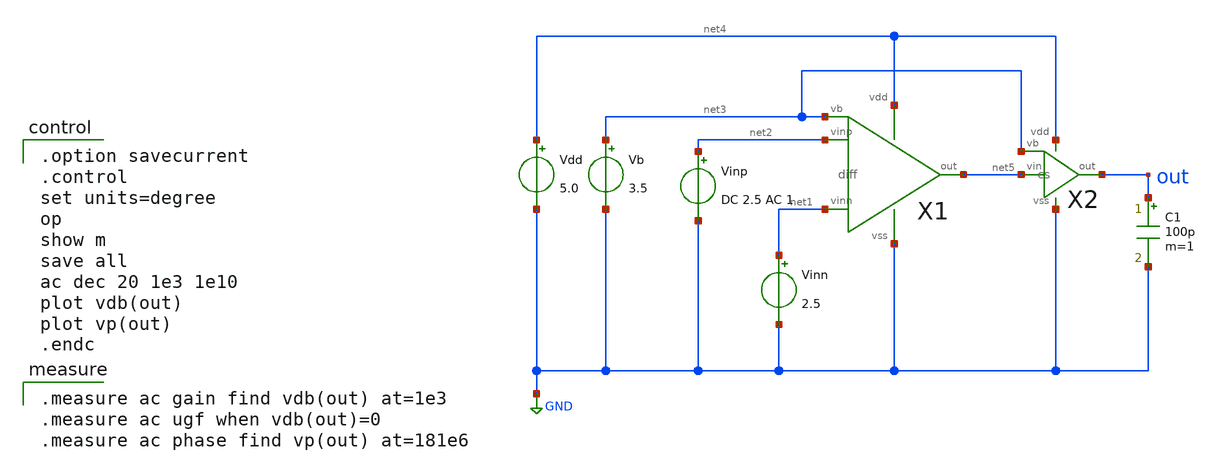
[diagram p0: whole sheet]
** sch_path: OpenSUSI-TR10/opamp/2stage_ac.sch
**.subckt 2stage_ac
Vdd net4 GND 5.0
Vb net3 GND 3.5
Vinp net2 GND DC 2.5 AC 1
X1 net2 net1 net5 net4 GND net3 diff
X2 net5 net3 out net4 GND cs
C1 out GND 100p m=1
Vinn net1 GND 2.5
**** begin user architecture code

.option savecurrent
.control
set units=degree
op
show m
save all
ac dec 20 1e3 1e10
plot vdb(out)
plot vp(out)
.endc


.measure ac gain find vdb(out) at=1e3
.measure ac ugf when vdb(out)=0
.measure ac phase find vp(out) at=181e6

 .include $::LIB/ip62_models
**** end user architecture code
**.ends

* expanding   symbol:  diff.sym # of pins=6
** sym_path: diff.sym
** sch_path: diff.sch
.subckt diff vinp vinn out vdd vss vb
*.ipin vinn
*.ipin vinp
*.ipin vb
*.opin out
*.iopin vdd
*.iopin vss
M5 net2 vb vdd vdd pmos L=2u W=40u m=1
M1 net1 vinn net2 net2 pmos L=2u W=200u m=1
M2 out vinp net2 net2 pmos L=2u W=200u m=1
M3 net1 net1 vss vss nmos L=2u W=10u m=1
M4 out net1 vss vss nmos L=2u W=10u m=1
.ends


* expanding   symbol:  cs.sym # of pins=5
** sym_path: cs.sym
** sch_path: cs.sch
.subckt cs vin vb out vdd vss
*.ipin vb
*.ipin vin
*.opin out
*.iopin vss
*.iopin vdd
XM6 out vb vdd vdd PMOS w=270u l=1u as=0 ad=0 ps=0 pd=0 nrd=0 nrs=0 m=1
XM7 out vin vss vss NMOS w=90u l=1u as=0 ad=0 ps=0 pd=0 nrd=0 nrs=0 m=1
.ends

.GLOBAL GND
.end
